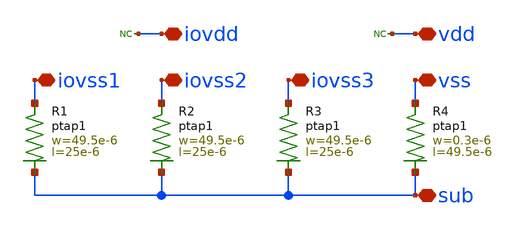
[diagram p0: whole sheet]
** sch_path: MSPHY6034-main/schematic/xschem/openpdk-libraries/ihp-sg13g2/sg13g2_io/xschem/sg13g2_Filler10000.sch
**.subckt sg13g2_Filler10000 iovss1 iovss2 iovss3 vss iovdd vdd sub
*.iopin iovss1
*.iopin iovss2
*.iopin iovss3
*.iopin vss
*.iopin iovdd
*.iopin vdd
*.iopin sub
XR3 iovss3 sub ptap1 R=706.8m w=49.5e-6 l=25e-6
XR4 vss sub ptap1 R=8.563 w=0.3e-6 l=49.5e-6
* noconn iovdd
* noconn vdd
XR1 iovss1 sub ptap1 R=706.8m w=49.5e-6 l=25e-6
XR2 iovss2 sub ptap1 R=706.8m w=49.5e-6 l=25e-6
**.ends
.end
